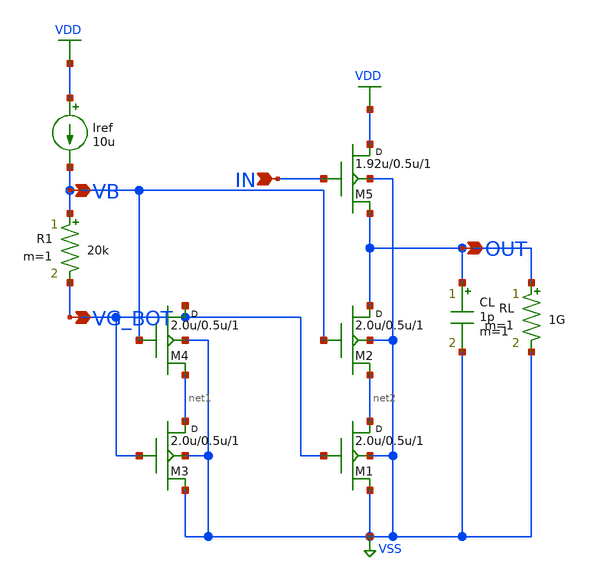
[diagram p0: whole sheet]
** sch_path: E3_238_Analog_VLSI_Circuits/05_Amplifier_Design/Problem_1_Source_Follower/source_follower.sch
**.subckt source_follower IN OUT VB VG_BOT
*.ipin IN
*.opin OUT
*.opin VB
*.opin VG_BOT
Iref VDD VB 10u
R1 VB VG_BOT 20k m=1
M4 VG_BOT VB net1 VSS nmos w=2.0u l=0.5u m=1
M3 net1 VG_BOT VSS VSS nmos w=2.0u l=0.5u m=1
M5 VDD IN OUT VSS nmos w=1.92u l=0.5u m=1
M2 OUT VB net2 VSS nmos w=2.0u l=0.5u m=1
M1 net2 VG_BOT VSS VSS nmos w=2.0u l=0.5u m=1
CL OUT VSS 1p m=1
RL OUT VSS 1G m=1
**** begin user architecture code

.include /home/anirudh/Analog_VLSI_Projects/models/cmos_180nm.mod
Vdd vdd 0 1.8
Vss vss 0 0
Vin in 0 1.25 AC 1.0

.control
  set color0=white
  set color1=black

  echo ""
  echo "==========================================================="
  echo "--- LAB 5 PROBLEM 1: DC OPERATING POINT & MEASUREMENTS ---"
  echo "==========================================================="
  op
  print v(IN) v(OUT) v(VB) v(VG_BOT)
  let V_error = v(OUT) - v(IN)
  let Vgs5 = v(IN) - v(OUT)
  print V_error Vgs5
  show m5 : gm gds gmbs id vgs vds vth
  show m2 : gm gds id vgs vds vth
  show m1 : gm gds id vgs vds vth

  echo ""
  echo "--- AC FREQUENCY RESPONSE ---"
  ac dec 30 1 10G
  meas ac gain_lf find vdb(OUT) at=1
  meas ac bw when vdb(OUT)=gain_lf-3 fall=1
  print gain_lf bw
  plot vdb(OUT) title 'Source Follower AC Gain (dB20) vs Frequency'
.endc


**** end user architecture code
**.ends
.GLOBAL VDD
.GLOBAL VSS
.end
